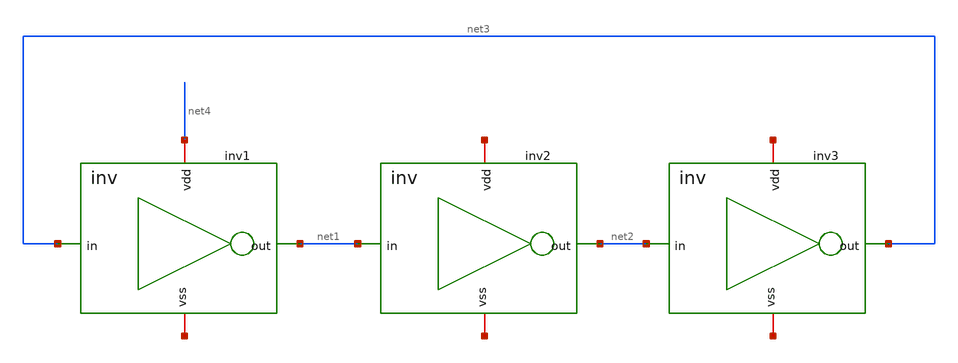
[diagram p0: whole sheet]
** sch_path: designs/library/ring_osc/ring_osc_3stg.sch
**.subckt ring_osc_3stg
inv1 net4 net3 net1 net5 inv
inv2 net6 net1 net2 net7 inv
inv3 net8 net2 net3 net9 inv
**.ends

* expanding   symbol:  /foss/designs/library/ring_osc/inv.sym # of pins=4
** sym_path: designs/library/ring_osc/inv.sym
** sch_path: designs/library/ring_osc/inv.sch
.subckt inv vdd in out vss
*.ipin in
*.opin out
*.iopin vdd
*.iopin vss
XM1 out in vss vss nfet_03v3 L=0.28u W=0.22u nf=1 ad='int((nf+1)/2) * W/nf * 0.18u' as='int((nf+2)/2) * W/nf * 0.18u'
+ pd='2*int((nf+1)/2) * (W/nf + 0.18u)' ps='2*int((nf+2)/2) * (W/nf + 0.18u)' nrd='0.18u / W' nrs='0.18u / W'
+ sa=0 sb=0 sd=0 m=1
XM2 out in vdd vdd pfet_03v3 L=0.28u W=0.22u nf=1 ad='int((nf+1)/2) * W/nf * 0.18u' as='int((nf+2)/2) * W/nf * 0.18u'
+ pd='2*int((nf+1)/2) * (W/nf + 0.18u)' ps='2*int((nf+2)/2) * (W/nf + 0.18u)' nrd='0.18u / W' nrs='0.18u / W'
+ sa=0 sb=0 sd=0 m=1
.ends

.end
